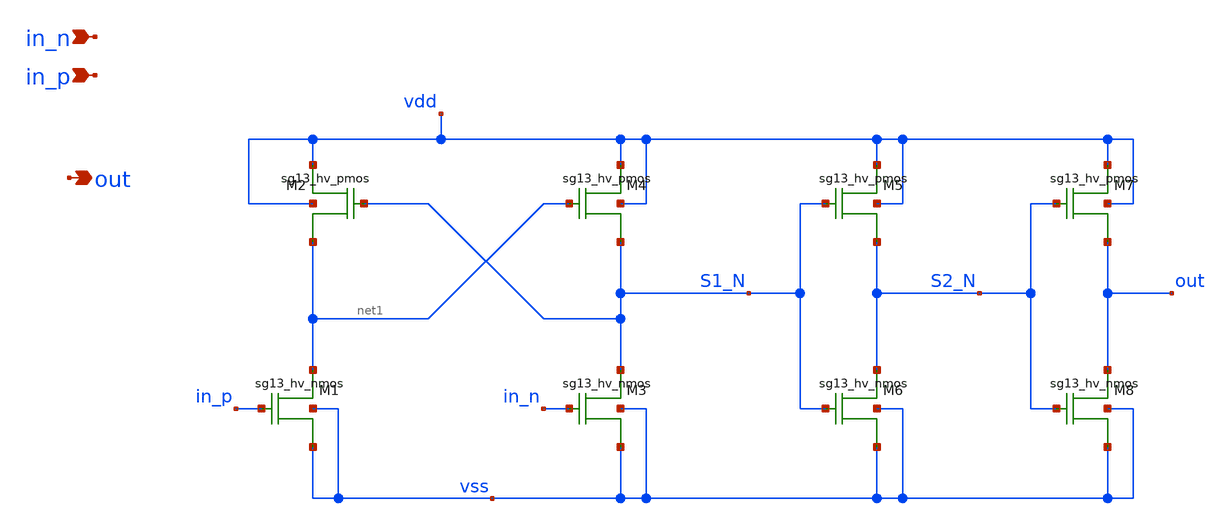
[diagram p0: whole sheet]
** sch_path: previous/level_shift.sch
**.subckt level_shift in_n in_p out
*.ipin in_n
*.ipin in_p
*.opin out
XM1 net1 in_p vss vss sg13_hv_nmos w=4u l=0.5u ng=1 m=2
XM2 vdd S1_N net1 vdd sg13_hv_pmos w=1u l=0.5u ng=1 m=2
XM3 S1_N in_n vss vss sg13_hv_nmos w=4u l=0.5u ng=1 m=2
XM4 vdd net1 S1_N vdd sg13_hv_pmos w=1u l=0.5u ng=1 m=2
XM5 vdd S1_N S2_N vdd sg13_hv_pmos w=2u l=0.5u ng=1 m=2
XM6 S2_N S1_N vss vss sg13_hv_nmos w=1u l=0.5u ng=1 m=2
XM7 vdd S2_N out vdd sg13_hv_pmos w=2u l=0.5u ng=1 m=4
XM8 out S2_N vss vss sg13_hv_nmos w=1u l=0.5u ng=1 m=4
**.ends
.end
